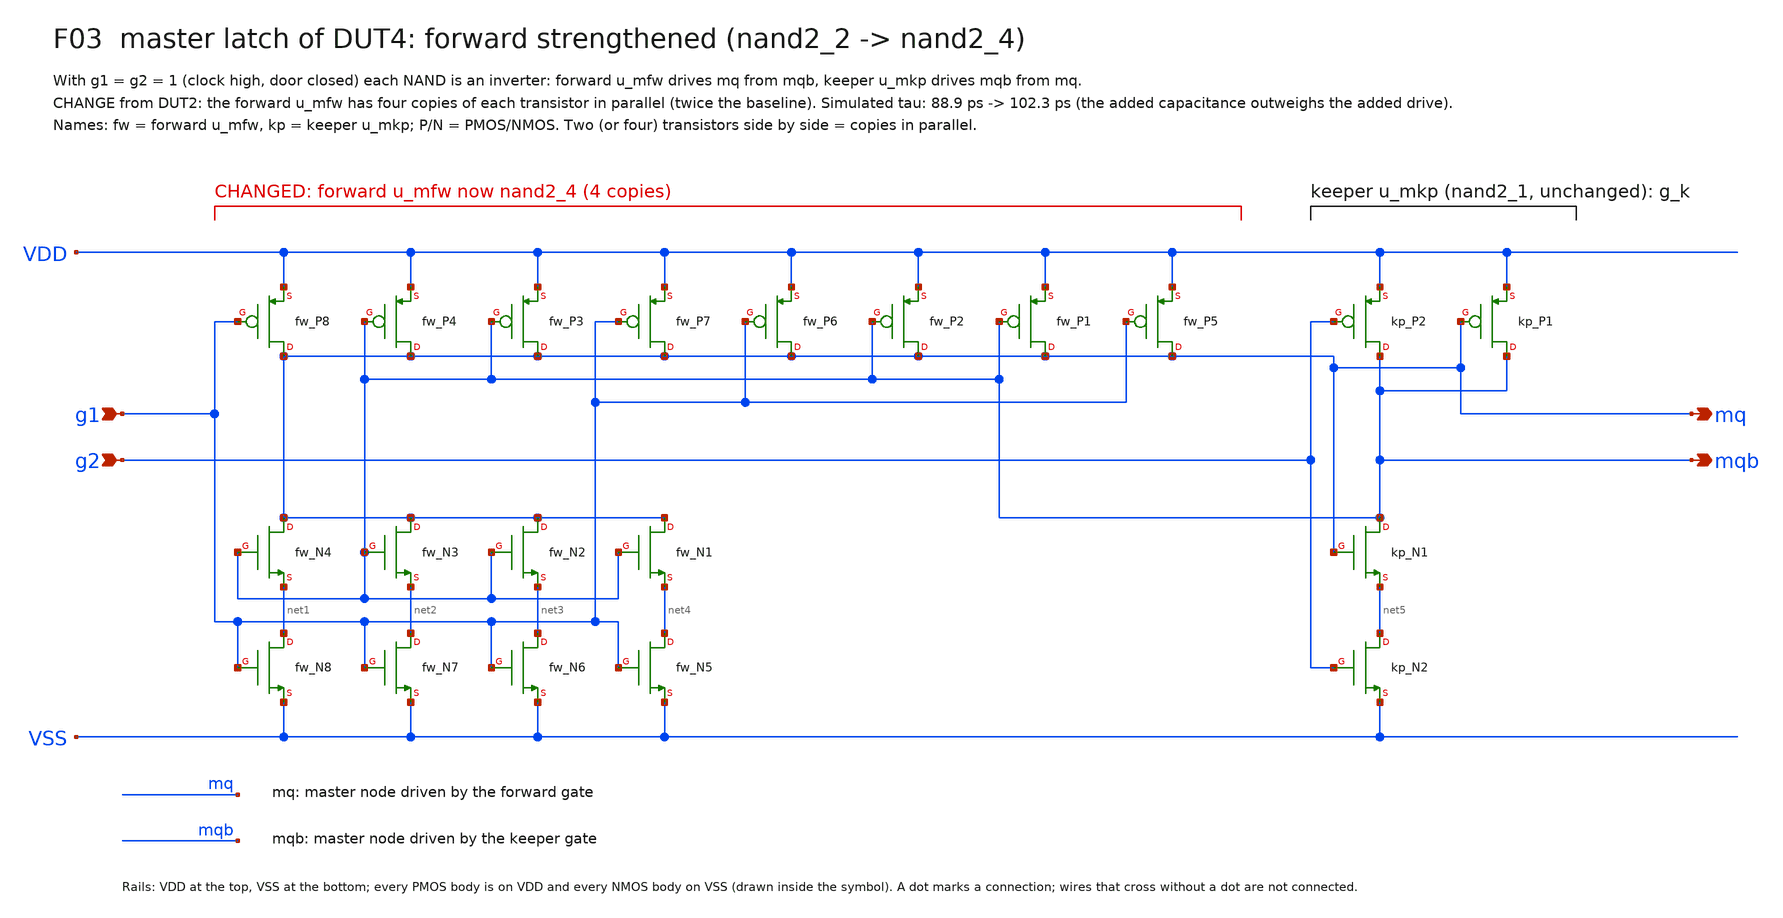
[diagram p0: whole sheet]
** sch_path: xschem/focus/F03_master_latch_forward.sch
**.subckt F03_master_latch_forward g1 g2 mq mqb
*.ipin g1
*.ipin g2
*.opin mq
*.opin mqb
Xfw_N8 net1 g1 VSS VSS nfet_05v0 L=0.6u W=0.82u nf=1 m=1
Xfw_N4 mq mqb net1 VSS nfet_05v0 L=0.6u W=0.82u nf=1 m=1
Xfw_N3 mq mqb net2 VSS nfet_05v0 L=0.6u W=0.82u nf=1 m=1
Xfw_N7 net2 g1 VSS VSS nfet_05v0 L=0.6u W=0.82u nf=1 m=1
Xfw_N6 net3 g1 VSS VSS nfet_05v0 L=0.6u W=0.82u nf=1 m=1
Xfw_N2 mq mqb net3 VSS nfet_05v0 L=0.6u W=0.82u nf=1 m=1
Xfw_N1 mq mqb net4 VSS nfet_05v0 L=0.6u W=0.82u nf=1 m=1
Xfw_N5 net4 g1 VSS VSS nfet_05v0 L=0.6u W=0.82u nf=1 m=1
Xfw_P8 mq g1 VDD VDD pfet_05v0 L=0.5u W=1.13u nf=1 m=1
Xfw_P4 mq mqb VDD VDD pfet_05v0 L=0.5u W=1.13u nf=1 m=1
Xfw_P3 mq mqb VDD VDD pfet_05v0 L=0.5u W=1.13u nf=1 m=1
Xfw_P7 mq g1 VDD VDD pfet_05v0 L=0.5u W=1.13u nf=1 m=1
Xfw_P6 mq g1 VDD VDD pfet_05v0 L=0.5u W=1.13u nf=1 m=1
Xfw_P2 mq mqb VDD VDD pfet_05v0 L=0.5u W=1.13u nf=1 m=1
Xfw_P1 mq mqb VDD VDD pfet_05v0 L=0.5u W=1.13u nf=1 m=1
Xfw_P5 mq g1 VDD VDD pfet_05v0 L=0.5u W=1.13u nf=1 m=1
Xkp_N2 net5 g2 VSS VSS nfet_05v0 L=0.6u W=0.82u nf=1 m=1
Xkp_N1 mqb mq net5 VSS nfet_05v0 L=0.6u W=0.82u nf=1 m=1
Xkp_P2 mqb g2 VDD VDD pfet_05v0 L=0.5u W=1.13u nf=1 m=1
Xkp_P1 mqb mq VDD VDD pfet_05v0 L=0.5u W=1.13u nf=1 m=1
**.ends
.end
